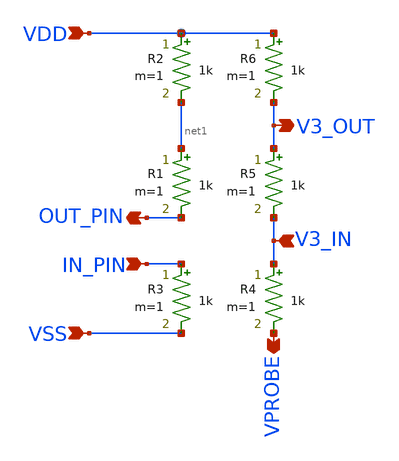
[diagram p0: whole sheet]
** sch_path: design/JNW_GR03_SKY130A/CURRENT_DEMO.sch
**.subckt CURRENT_DEMO VSS VDD VPROBE OUT_PIN IN_PIN V3_OUT V3_IN
*.ipin VSS
*.ipin VDD
*.opin VPROBE
*.opin OUT_PIN
*.ipin IN_PIN
*.opin V3_OUT
*.ipin V3_IN
R1 net1 OUT_PIN 1k m=1
R2 VDD net1 1k m=1
R3 IN_PIN VSS 1k m=1
R4 V3_IN VPROBE 1k m=1
R5 V3_OUT V3_IN 1k m=1
R6 VDD V3_OUT 1k m=1
**.ends
.end
